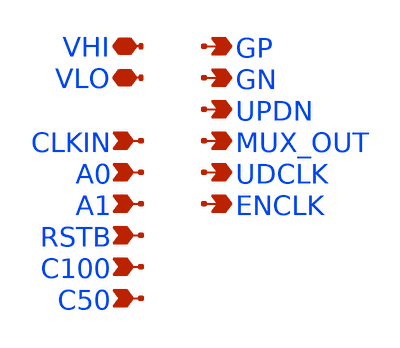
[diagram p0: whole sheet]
** sch_path: xschem/twcon_PEX.sch
**.subckt twcon_PEX VHI VLO UPDN CLKIN A0 A1 RSTB C100 C50 GP GN MUX_OUT UDCLK ENCLK
*.iopin VHI
*.iopin VLO
*.opin UPDN
*.ipin CLKIN
*.ipin A0
*.ipin A1
*.ipin RSTB
*.ipin C100
*.ipin C50
*.opin GP
*.opin GN
*.opin MUX_OUT
*.opin UDCLK
*.opin ENCLK
**** begin user architecture code

* NGSPICE file created from twcon.ext - technology: sky130A
.subckt twcon VHI VLO UPDN CLKIN A0 A1 GP GN RSTB C100 C50 MUX_OUT UDCLK ENCLK

* NGSPICE file created from twcon_flat.ext - technology: sky130A

X0 a_533_410# VLO VLO VLO sky130_fd_pr__nfet_01v8_lvt ad=0p pd=0u as=0p ps=0u w=420000u l=150000u
X1 VLO a_533_410# a_555_119# VLO sky130_fd_pr__nfet_01v8_lvt ad=0p pd=0u as=0p ps=0u w=420000u
+ l=150000u
X2 a_1346_464# a_1060_368# a_1262_464# w_n2918_628# sky130_fd_pr__pfet_01v8 ad=0p pd=0u as=0p ps=0u
+ w=420000u l=150000u
X3 VHI VLO VHI w_n2918_1664# sky130_fd_pr__pfet_01v8 ad=0p pd=0u as=0p ps=0u w=1e+06u l=1e+06u
X4 a_1377_125# a_1199_366# VLO VLO sky130_fd_pr__nfet_01v8_lvt ad=0p pd=0u as=0p ps=0u w=420000u
+ l=150000u
X5 a_n2680_1700# a_n1984_1467# VLO sky130_fd_pr__res_xhigh_po_1p41 l=500000u
X6 a_2189_82# a_1060_368# a_2178_424# w_n2918_628# sky130_fd_pr__pfet_01v8 ad=0p pd=0u as=0p ps=0u
+ w=840000u l=150000u
X7 VHI VLO a_219_464# w_n2918_628# sky130_fd_pr__pfet_01v8 ad=0p pd=0u as=0p ps=0u w=640000u
+ l=150000u
X8 a_n1326_740# a_n1984_915# VHI w_n2918_628# sky130_fd_pr__pfet_01v8 ad=0p pd=0u as=0p ps=0u
+ w=1.12e+06u l=150000u
X9 a_2363_740# a_880_1086# a_2189_1140# w_n2918_628# sky130_fd_pr__pfet_01v8 ad=0p pd=0u as=0p ps=0u
+ w=420000u l=150000u
X10 VHI a_3464_1110# a_3664_740# w_n2918_628# sky130_fd_pr__pfet_01v8 ad=0p pd=0u as=0p ps=0u
+ w=1.12e+06u l=150000u
X11 MUX_OUT a_n848_1110# VLO VLO sky130_fd_pr__nfet_01v8_lvt ad=0p pd=0u as=0p ps=0u w=740000u
+ l=150000u
X12 VHI A0 a_n1326_740# w_n2918_628# sky130_fd_pr__pfet_01v8 ad=0p pd=0u as=0p ps=0u w=1.12e+06u
+ l=150000u
X13 a_1262_464# a_1199_366# VHI w_n2918_628# sky130_fd_pr__pfet_01v8 ad=0p pd=0u as=0p ps=0u
+ w=420000u l=150000u
X14 a_3664_740# a_3464_1110# VHI w_n2918_628# sky130_fd_pr__pfet_01v8 ad=0p pd=0u as=0p ps=0u
+ w=1.12e+06u l=150000u
X15 VHI VLO VHI w_n2918_1664# sky130_fd_pr__pfet_01v8 ad=0p pd=0u as=0p ps=0u w=1e+06u l=1e+06u
X16 VLO VHI VLO VLO sky130_fd_pr__nfet_01v8_lvt ad=0p pd=0u as=0p ps=0u w=420000u l=1e+06u
X17 a_4149_409# a_n1069_979# a_4146_119# VLO sky130_fd_pr__nfet_01v8_lvt ad=0p pd=0u as=0p ps=0u
+ w=640000u l=150000u
X18 VLO UPDN a_4059_1110# VLO sky130_fd_pr__nfet_01v8_lvt ad=0p pd=0u as=0p ps=0u w=740000u
+ l=150000u
X19 a_2189_82# a_880_98# a_2094_125# VLO sky130_fd_pr__nfet_01v8_lvt ad=0p pd=0u as=0p ps=0u
+ w=550000u l=150000u
X20 a_n1750_2358# a_n1984_915# sky130_fd_pr__cap_mim_m3_2 l=1.6e+06u w=1.57e+07u
X21 GN a_4149_409# VLO VLO sky130_fd_pr__nfet_01v8_lvt ad=0p pd=0u as=0p ps=0u w=740000u l=150000u
X22 a_n1323_1406# a_n1984_1467# VLO VLO sky130_fd_pr__nfet_01v8_lvt ad=0p pd=0u as=0p ps=0u
+ w=740000u l=150000u
X23 a_219_740# a_533_883# a_389_1129# w_n2918_628# sky130_fd_pr__pfet_01v8 ad=0p pd=0u as=0p ps=0u
+ w=640000u l=150000u
X24 a_389_1129# VLO a_311_1129# VLO sky130_fd_pr__nfet_01v8_lvt ad=0p pd=0u as=0p ps=0u w=420000u
+ l=150000u
X25 a_1060_740# a_880_1086# VLO VLO sky130_fd_pr__nfet_01v8_lvt ad=0p pd=0u as=0p ps=0u w=740000u
+ l=150000u
X26 a_2189_1140# a_1060_740# a_2178_740# w_n2918_628# sky130_fd_pr__pfet_01v8 ad=0p pd=0u as=0p
+ ps=0u w=840000u l=150000u
X27 a_2408_839# a_2189_1140# a_2748_740# w_n2918_628# sky130_fd_pr__pfet_01v8 ad=0p pd=0u as=0p
+ ps=0u w=1e+06u l=150000u
X28 a_n1528_368# CLKIN VHI w_n2918_628# sky130_fd_pr__pfet_01v8 ad=0p pd=0u as=0p ps=0u w=1.12e+06u
+ l=150000u
X29 a_n832_135# a_n1313_n698# sky130_fd_pr__cap_mim_m3_1 l=1.6e+06u w=7.85e+06u
X30 a_4146_119# a_3664_740# VLO VLO sky130_fd_pr__nfet_01v8_lvt ad=0p pd=0u as=0p ps=0u w=640000u
+ l=150000u
X31 a_555_119# a_n1069_979# a_389_119# VLO sky130_fd_pr__nfet_01v8_lvt ad=0p pd=0u as=0p ps=0u
+ w=420000u l=150000u
X32 VHI a_n1125_796# a_n628_764# w_n2918_628# sky130_fd_pr__pfet_01v8 ad=0p pd=0u as=0p ps=0u
+ w=1e+06u l=150000u
X33 a_n709_1110# a_n1326_740# a_n848_1110# VLO sky130_fd_pr__nfet_01v8_lvt ad=0p pd=0u as=0p ps=0u
+ w=740000u l=150000u
X34 a_389_1129# VHI a_398_740# w_n2918_628# sky130_fd_pr__pfet_01v8 ad=0p pd=0u as=0p ps=0u
+ w=640000u l=150000u
X35 a_4059_1110# a_3664_740# GP VLO sky130_fd_pr__nfet_01v8_lvt ad=0p pd=0u as=0p ps=0u w=740000u
+ l=150000u
X36 VLO VHI a_1665_73# VLO sky130_fd_pr__nfet_01v8_lvt ad=0p pd=0u as=0p ps=0u w=550000u l=150000u
X37 a_2178_424# a_1199_366# VHI w_n2918_628# sky130_fd_pr__pfet_01v8 ad=0p pd=0u as=0p ps=0u
+ w=840000u l=150000u
X38 VHI UPDN GP w_n2918_628# sky130_fd_pr__pfet_01v8 ad=0p pd=0u as=0p ps=0u w=1.12e+06u l=150000u
X39 VHI a_n1069_979# a_n1125_796# w_n2918_628# sky130_fd_pr__pfet_01v8 ad=0p pd=0u as=0p ps=0u
+ w=840000u l=150000u
X40 VLO a_3464_1110# a_3664_740# VLO sky130_fd_pr__nfet_01v8_lvt ad=0p pd=0u as=0p ps=0u w=740000u
+ l=150000u
X41 VLO VHI VLO VLO sky130_fd_pr__nfet_01v8_lvt ad=0p pd=0u as=0p ps=0u w=420000u l=1e+06u
X42 a_4059_1110# UPDN VLO VLO sky130_fd_pr__nfet_01v8_lvt ad=0p pd=0u as=0p ps=0u w=740000u
+ l=150000u
X43 VHI VHI a_2408_839# w_n2918_628# sky130_fd_pr__pfet_01v8 ad=0p pd=0u as=0p ps=0u w=1e+06u
+ l=150000u
X44 VLO C100 a_n1750_3072# VLO sky130_fd_pr__nfet_01v8 ad=0p pd=0u as=0p ps=0u w=2e+06u l=150000u
X45 VLO a_2408_839# a_3464_1110# VLO sky130_fd_pr__nfet_01v8_lvt ad=0p pd=0u as=0p ps=0u w=640000u
+ l=150000u
X46 a_n832_135# a_n1313_n1412# sky130_fd_pr__cap_mim_m3_1 l=1.6e+06u w=1.57e+07u
X47 a_n1069_979# a_2408_410# VLO VLO sky130_fd_pr__nfet_01v8_lvt ad=0p pd=0u as=0p ps=0u w=740000u
+ l=150000u
X48 VHI A1 a_n1326_1700# w_n2918_1664# sky130_fd_pr__pfet_01v8 ad=0p pd=0u as=0p ps=0u w=1.12e+06u
+ l=150000u
X49 VHI a_4149_409# GN w_n2918_628# sky130_fd_pr__pfet_01v8 ad=0p pd=0u as=0p ps=0u w=1.12e+06u
+ l=150000u
X50 VLO ENCLK a_880_1086# VLO sky130_fd_pr__nfet_01v8_lvt ad=0p pd=0u as=0p ps=0u w=740000u
+ l=150000u
X51 a_389_1129# a_880_1086# a_1346_784# w_n2918_628# sky130_fd_pr__pfet_01v8 ad=0p pd=0u as=0p ps=0u
+ w=640000u l=150000u
X52 VLO a_2408_839# a_3253_1110# VLO sky130_fd_pr__nfet_01v8_lvt ad=0p pd=0u as=0p ps=0u w=740000u
+ l=150000u
X53 VHI a_2408_839# a_3464_1110# w_n2918_628# sky130_fd_pr__pfet_01v8 ad=0p pd=0u as=0p ps=0u
+ w=1e+06u l=150000u
X54 a_n880_2358# C50 VLO VLO sky130_fd_pr__nfet_01v8 ad=0p pd=0u as=0p ps=0u w=2e+06u l=150000u
X55 VLO CLKIN ENCLK VLO sky130_fd_pr__nfet_01v8_lvt ad=0p pd=0u as=0p ps=0u w=740000u l=150000u
X56 a_2748_740# a_1835_923# VHI w_n2918_628# sky130_fd_pr__pfet_01v8 ad=0p pd=0u as=0p ps=0u
+ w=1e+06u l=150000u
X57 a_n1326_1700# A1 a_n1323_1406# VLO sky130_fd_pr__nfet_01v8_lvt ad=0p pd=0u as=0p ps=0u w=740000u
+ l=150000u
X58 VLO VHI VLO VLO sky130_fd_pr__nfet_01v8_lvt ad=0p pd=0u as=0p ps=0u w=420000u l=1e+06u
X59 VLO UPDN a_4059_1110# VLO sky130_fd_pr__nfet_01v8_lvt ad=0p pd=0u as=0p ps=0u w=740000u
+ l=150000u
X60 VHI MUX_OUT a_1835_923# w_n2918_628# sky130_fd_pr__pfet_01v8 ad=0p pd=0u as=0p ps=0u w=640000u
+ l=150000u
X61 VHI a_2408_839# a_3253_1110# w_n2918_628# sky130_fd_pr__pfet_01v8 ad=0p pd=0u as=0p ps=0u
+ w=1.12e+06u l=150000u
X62 VHI VLO VHI w_n2918_1664# sky130_fd_pr__pfet_01v8 ad=0p pd=0u as=0p ps=0u w=1e+06u l=1e+06u
X63 a_2178_740# a_1199_900# VHI w_n2918_628# sky130_fd_pr__pfet_01v8 ad=0p pd=0u as=0p ps=0u
+ w=840000u l=150000u
X64 a_n2680_1700# A1 VLO VLO sky130_fd_pr__nfet_01v8_lvt ad=0p pd=0u as=0p ps=0u w=740000u l=150000u
X65 VLO VHI VLO VLO sky130_fd_pr__nfet_01v8_lvt ad=0p pd=0u as=0p ps=0u w=420000u l=1e+06u
X66 a_2644_74# VHI VLO VLO sky130_fd_pr__nfet_01v8_lvt ad=0p pd=0u as=0p ps=0u w=740000u l=150000u
X67 a_n1326_1700# a_n1984_1467# VHI w_n2918_1664# sky130_fd_pr__pfet_01v8 ad=0p pd=0u as=0p ps=0u
+ w=1.12e+06u l=150000u
X68 VLO VHI VLO VLO sky130_fd_pr__nfet_01v8_lvt ad=0p pd=0u as=0p ps=0u w=420000u l=1e+06u
X69 VHI a_3664_740# a_4149_409# w_n2918_628# sky130_fd_pr__pfet_01v8 ad=0p pd=0u as=0p ps=0u
+ w=840000u l=150000u
X70 VLO VHI VLO VLO sky130_fd_pr__nfet_01v8_lvt ad=0p pd=0u as=0p ps=0u w=420000u l=1e+06u
X71 a_n628_764# a_n1326_1700# a_n848_1110# w_n2918_628# sky130_fd_pr__pfet_01v8 ad=0p pd=0u as=0p
+ ps=0u w=1e+06u l=150000u
X72 a_3253_1110# a_2408_839# VHI w_n2918_628# sky130_fd_pr__pfet_01v8 ad=0p pd=0u as=0p ps=0u
+ w=1.12e+06u l=150000u
X73 UDCLK CLKIN a_n171_74# VLO sky130_fd_pr__nfet_01v8_lvt ad=0p pd=0u as=0p ps=0u w=740000u
+ l=150000u
X74 a_398_740# VLO VHI w_n2918_628# sky130_fd_pr__pfet_01v8 ad=0p pd=0u as=0p ps=0u w=640000u
+ l=150000u
X75 a_n1984_1467# a_n880_3072# sky130_fd_pr__cap_mim_m3_1 l=1.6e+06u w=7.85e+06u
X76 VLO VHI VLO VLO sky130_fd_pr__nfet_01v8_lvt ad=0p pd=0u as=0p ps=0u w=420000u l=1e+06u
X77 ENCLK CLKIN VHI w_n2918_628# sky130_fd_pr__pfet_01v8 ad=0p pd=0u as=0p ps=0u w=1.12e+06u
+ l=150000u
X78 a_2408_839# a_1835_923# a_2644_1110# VLO sky130_fd_pr__nfet_01v8_lvt ad=0p pd=0u as=0p ps=0u
+ w=740000u l=150000u
X79 VLO VHI VLO VLO sky130_fd_pr__nfet_01v8_lvt ad=0p pd=0u as=0p ps=0u w=420000u l=1e+06u
X80 ENCLK CLKIN VLO VLO sky130_fd_pr__nfet_01v8_lvt ad=0p pd=0u as=0p ps=0u w=740000u l=150000u
X81 a_4059_1110# UPDN VLO VLO sky130_fd_pr__nfet_01v8_lvt ad=0p pd=0u as=0p ps=0u w=740000u
+ l=150000u
X82 a_n1313_n698# a_n832_135# sky130_fd_pr__cap_mim_m3_2 l=1.6e+06u w=7.85e+06u
X83 VHI VLO a_219_740# w_n2918_628# sky130_fd_pr__pfet_01v8 ad=0p pd=0u as=0p ps=0u w=640000u
+ l=150000u
X84 a_3664_740# a_3464_1110# VLO VLO sky130_fd_pr__nfet_01v8_lvt ad=0p pd=0u as=0p ps=0u w=740000u
+ l=150000u
X85 VHI CLKIN ENCLK w_n2918_628# sky130_fd_pr__pfet_01v8 ad=0p pd=0u as=0p ps=0u w=1.12e+06u
+ l=150000u
X86 GP a_3664_740# a_4059_1110# VLO sky130_fd_pr__nfet_01v8_lvt ad=0p pd=0u as=0p ps=0u w=740000u
+ l=150000u
X87 VLO VHI VLO VLO sky130_fd_pr__nfet_01v8_lvt ad=0p pd=0u as=0p ps=0u w=420000u l=1e+06u
X88 VHI a_3464_94# UPDN w_n2918_628# sky130_fd_pr__pfet_01v8 ad=0p pd=0u as=0p ps=0u w=1.12e+06u
+ l=150000u
X89 a_n848_1110# a_n1326_740# a_n929_764# w_n2918_628# sky130_fd_pr__pfet_01v8 ad=0p pd=0u as=0p
+ ps=0u w=1e+06u l=150000u
X90 VLO a_2408_410# a_n1069_979# VLO sky130_fd_pr__nfet_01v8_lvt ad=0p pd=0u as=0p ps=0u w=740000u
+ l=150000u
X91 a_1060_368# a_880_98# VLO VLO sky130_fd_pr__nfet_01v8_lvt ad=0p pd=0u as=0p ps=0u w=740000u
+ l=150000u
X92 VHI VLO VHI w_n2918_1664# sky130_fd_pr__pfet_01v8 ad=0p pd=0u as=0p ps=0u w=1e+06u l=1e+06u
X93 a_2189_1140# a_880_1086# a_2094_1097# VLO sky130_fd_pr__nfet_01v8_lvt ad=0p pd=0u as=0p ps=0u
+ w=550000u l=150000u
X94 a_2644_1110# a_2189_1140# a_2408_839# VLO sky130_fd_pr__nfet_01v8_lvt ad=0p pd=0u as=0p ps=0u
+ w=740000u l=150000u
X95 VHI RSTB a_1835_257# w_n2918_628# sky130_fd_pr__pfet_01v8 ad=0p pd=0u as=0p ps=0u w=640000u
+ l=150000u
X96 a_n1313_n1412# a_n832_135# sky130_fd_pr__cap_mim_m3_2 l=1.6e+06u w=1.57e+07u
X97 UPDN a_3464_94# VHI w_n2918_628# sky130_fd_pr__pfet_01v8 ad=0p pd=0u as=0p ps=0u w=1.12e+06u
+ l=150000u
X98 a_3253_1110# a_2408_839# VLO VLO sky130_fd_pr__nfet_01v8_lvt ad=0p pd=0u as=0p ps=0u w=740000u
+ l=150000u
X99 VHI VLO VHI w_n2918_1664# sky130_fd_pr__pfet_01v8 ad=0p pd=0u as=0p ps=0u w=1e+06u l=1e+06u
X100 VLO a_533_883# a_555_1129# VLO sky130_fd_pr__nfet_01v8_lvt ad=0p pd=0u as=0p ps=0u w=420000u
+ l=150000u
X101 a_2439_82# a_1060_368# a_2189_82# VLO sky130_fd_pr__nfet_01v8_lvt ad=0p pd=0u as=0p ps=0u
+ w=420000u l=150000u
X102 a_1377_1123# a_1199_900# VLO VLO sky130_fd_pr__nfet_01v8_lvt ad=0p pd=0u as=0p ps=0u w=420000u
+ l=150000u
X103 a_1346_784# a_1060_740# a_1262_784# w_n2918_628# sky130_fd_pr__pfet_01v8 ad=0p pd=0u as=0p
+ ps=0u w=420000u l=150000u
X104 a_n1313_n1412# C100 VLO VLO sky130_fd_pr__nfet_01v8 ad=0p pd=0u as=0p ps=0u w=2e+06u l=150000u
X105 VHI a_2408_410# a_2363_508# w_n2918_628# sky130_fd_pr__pfet_01v8 ad=0p pd=0u as=0p ps=0u
+ w=420000u l=150000u
X106 VLO UDCLK a_880_98# VLO sky130_fd_pr__nfet_01v8_lvt ad=0p pd=0u as=0p ps=0u w=740000u l=150000u
X107 a_n880_3072# C100 VLO VLO sky130_fd_pr__nfet_01v8 ad=0p pd=0u as=0p ps=0u w=2e+06u l=150000u
X108 a_n880_3072# a_n1984_1467# sky130_fd_pr__cap_mim_m3_2 l=1.6e+06u w=7.85e+06u
X109 a_2408_410# a_2189_82# a_2748_392# w_n2918_628# sky130_fd_pr__pfet_01v8 ad=0p pd=0u as=0p ps=0u
+ w=1e+06u l=150000u
X110 a_311_1129# VLO VLO VLO sky130_fd_pr__nfet_01v8_lvt ad=0p pd=0u as=0p ps=0u w=420000u l=150000u
X111 MUX_OUT a_n848_1110# VHI w_n2918_628# sky130_fd_pr__pfet_01v8 ad=0p pd=0u as=0p ps=0u
+ w=1.12e+06u l=150000u
X112 a_1262_784# a_1199_900# VHI w_n2918_628# sky130_fd_pr__pfet_01v8 ad=0p pd=0u as=0p ps=0u
+ w=420000u l=150000u
X113 a_533_410# VLO VHI w_n2918_628# sky130_fd_pr__pfet_01v8 ad=0p pd=0u as=0p ps=0u w=640000u
+ l=150000u
X114 a_n1984_1467# a_n880_2358# sky130_fd_pr__cap_mim_m3_1 l=1.6e+06u w=1.57e+07u
X115 a_1199_366# a_1346_464# a_1665_73# VLO sky130_fd_pr__nfet_01v8_lvt ad=0p pd=0u as=0p ps=0u
+ w=550000u l=150000u
X116 a_555_1129# VHI a_389_1129# VLO sky130_fd_pr__nfet_01v8_lvt ad=0p pd=0u as=0p ps=0u w=420000u
+ l=150000u
X117 VHI VHI a_2408_410# w_n2918_628# sky130_fd_pr__pfet_01v8 ad=0p pd=0u as=0p ps=0u w=1e+06u
+ l=150000u
X118 VHI a_1835_257# a_1784_424# w_n2918_628# sky130_fd_pr__pfet_01v8 ad=0p pd=0u as=0p ps=0u
+ w=840000u l=150000u
X119 a_n1528_368# CLKIN VLO VLO sky130_fd_pr__nfet_01v8_lvt ad=0p pd=0u as=0p ps=0u w=740000u
+ l=150000u
X120 a_n2680_740# A0 VHI w_n2918_628# sky130_fd_pr__pfet_01v8 ad=0p pd=0u as=0p ps=0u w=1.12e+06u
+ l=150000u
X121 a_n929_764# a_n1069_979# VHI w_n2918_628# sky130_fd_pr__pfet_01v8 ad=0p pd=0u as=0p ps=0u
+ w=1e+06u l=150000u
X122 a_2644_1110# VHI VLO VLO sky130_fd_pr__nfet_01v8_lvt ad=0p pd=0u as=0p ps=0u w=740000u
+ l=150000u
X123 a_2644_74# a_2189_82# a_2408_410# VLO sky130_fd_pr__nfet_01v8_lvt ad=0p pd=0u as=0p ps=0u
+ w=740000u l=150000u
X124 a_n2680_740# a_n1984_915# VLO sky130_fd_pr__res_xhigh_po_1p41 l=500000u
X125 a_1346_784# a_880_1086# a_1377_1123# VLO sky130_fd_pr__nfet_01v8_lvt ad=0p pd=0u as=0p ps=0u
+ w=420000u l=150000u
X126 a_2439_1166# a_1060_740# a_2189_1140# VLO sky130_fd_pr__nfet_01v8_lvt ad=0p pd=0u as=0p ps=0u
+ w=420000u l=150000u
X127 GN a_4149_409# VHI w_n2918_628# sky130_fd_pr__pfet_01v8 ad=0p pd=0u as=0p ps=0u w=1.12e+06u
+ l=150000u
X128 VHI ENCLK a_880_1086# w_n2918_628# sky130_fd_pr__pfet_01v8 ad=0p pd=0u as=0p ps=0u w=1.12e+06u
+ l=150000u
X129 VHI a_2408_410# a_n1069_979# w_n2918_628# sky130_fd_pr__pfet_01v8 ad=0p pd=0u as=0p ps=0u
+ w=1.12e+06u l=150000u
X130 a_2363_508# a_880_98# a_2189_82# w_n2918_628# sky130_fd_pr__pfet_01v8 ad=0p pd=0u as=0p ps=0u
+ w=420000u l=150000u
X131 a_n1313_n698# C50 VLO VLO sky130_fd_pr__nfet_01v8 ad=0p pd=0u as=0p ps=0u w=2e+06u l=150000u
X132 a_4059_1110# a_3664_740# GP VLO sky130_fd_pr__nfet_01v8_lvt ad=0p pd=0u as=0p ps=0u w=740000u
+ l=150000u
X133 a_n1984_915# a_n1750_3072# sky130_fd_pr__cap_mim_m3_1 l=1.6e+06u w=7.85e+06u
X134 UPDN a_3464_94# VLO VLO sky130_fd_pr__nfet_01v8_lvt ad=0p pd=0u as=0p ps=0u w=740000u l=150000u
X135 a_2748_392# a_1835_257# VHI w_n2918_628# sky130_fd_pr__pfet_01v8 ad=0p pd=0u as=0p ps=0u
+ w=1e+06u l=150000u
X136 a_2094_125# a_1199_366# VLO VLO sky130_fd_pr__nfet_01v8_lvt ad=0p pd=0u as=0p ps=0u w=550000u
+ l=150000u
X137 VHI VLO VHI w_n2918_1664# sky130_fd_pr__pfet_01v8 ad=0p pd=0u as=0p ps=0u w=1e+06u l=1e+06u
X138 a_n1069_979# a_2408_410# VHI w_n2918_628# sky130_fd_pr__pfet_01v8 ad=0p pd=0u as=0p ps=0u
+ w=1.12e+06u l=150000u
X139 a_1060_740# a_880_1086# VHI w_n2918_628# sky130_fd_pr__pfet_01v8 ad=0p pd=0u as=0p ps=0u
+ w=1.12e+06u l=150000u
X140 a_1784_424# a_1346_464# a_1199_366# w_n2918_628# sky130_fd_pr__pfet_01v8 ad=0p pd=0u as=0p
+ ps=0u w=840000u l=150000u
X141 a_389_1129# a_1060_740# a_1346_784# VLO sky130_fd_pr__nfet_01v8_lvt ad=0p pd=0u as=0p ps=0u
+ w=420000u l=150000u
X142 VLO RSTB a_1835_257# VLO sky130_fd_pr__nfet_01v8_lvt ad=0p pd=0u as=0p ps=0u w=420000u
+ l=150000u
X143 UDCLK a_n832_135# VHI w_n2918_628# sky130_fd_pr__pfet_01v8 ad=0p pd=0u as=0p ps=0u w=1.12e+06u
+ l=150000u
X144 a_1199_366# VHI VHI w_n2918_628# sky130_fd_pr__pfet_01v8 ad=0p pd=0u as=0p ps=0u w=840000u
+ l=150000u
X145 VLO MUX_OUT a_1835_923# VLO sky130_fd_pr__nfet_01v8_lvt ad=0p pd=0u as=0p ps=0u w=420000u
+ l=150000u
X146 VLO VHI a_1665_1097# VLO sky130_fd_pr__nfet_01v8_lvt ad=0p pd=0u as=0p ps=0u w=550000u
+ l=150000u
X147 VHI a_1835_923# a_1784_740# w_n2918_628# sky130_fd_pr__pfet_01v8 ad=0p pd=0u as=0p ps=0u
+ w=840000u l=150000u
X148 a_389_119# VLO a_311_119# VLO sky130_fd_pr__nfet_01v8_lvt ad=0p pd=0u as=0p ps=0u w=420000u
+ l=150000u
X149 a_n2680_1700# A1 VHI w_n2918_1664# sky130_fd_pr__pfet_01v8 ad=0p pd=0u as=0p ps=0u w=1.12e+06u
+ l=150000u
X150 VLO VHI VLO VLO sky130_fd_pr__nfet_01v8_lvt ad=0p pd=0u as=0p ps=0u w=420000u l=1e+06u
X151 a_1199_900# a_1346_784# a_1665_1097# VLO sky130_fd_pr__nfet_01v8_lvt ad=0p pd=0u as=0p ps=0u
+ w=550000u l=150000u
X152 GN a_4149_409# VLO VLO sky130_fd_pr__nfet_01v8_lvt ad=0p pd=0u as=0p ps=0u w=740000u l=150000u
X153 VHI CLKIN UDCLK w_n2918_628# sky130_fd_pr__pfet_01v8 ad=0p pd=0u as=0p ps=0u w=1.12e+06u
+ l=150000u
X154 a_n1323_1110# a_n1984_915# VLO VLO sky130_fd_pr__nfet_01v8_lvt ad=0p pd=0u as=0p ps=0u
+ w=740000u l=150000u
X155 VLO a_2408_839# a_2439_1166# VLO sky130_fd_pr__nfet_01v8_lvt ad=0p pd=0u as=0p ps=0u w=420000u
+ l=150000u
X156 a_4149_409# a_n1069_979# VHI w_n2918_628# sky130_fd_pr__pfet_01v8 ad=0p pd=0u as=0p ps=0u
+ w=840000u l=150000u
X157 VHI VLO VHI w_n2918_1664# sky130_fd_pr__pfet_01v8 ad=0p pd=0u as=0p ps=0u w=1e+06u l=1e+06u
X158 VHI VLO VHI w_n2918_1664# sky130_fd_pr__pfet_01v8 ad=0p pd=0u as=0p ps=0u w=1e+06u l=1e+06u
X159 GP UPDN VHI w_n2918_628# sky130_fd_pr__pfet_01v8 ad=0p pd=0u as=0p ps=0u w=1.12e+06u l=150000u
X160 VHI VLO VHI w_n2918_1664# sky130_fd_pr__pfet_01v8 ad=0p pd=0u as=0p ps=0u w=1e+06u l=1e+06u
X161 a_533_883# VLO VLO VLO sky130_fd_pr__nfet_01v8_lvt ad=0p pd=0u as=0p ps=0u w=420000u l=150000u
X162 a_1784_740# a_1346_784# a_1199_900# w_n2918_628# sky130_fd_pr__pfet_01v8 ad=0p pd=0u as=0p
+ ps=0u w=840000u l=150000u
X163 a_n880_2358# a_n1984_1467# sky130_fd_pr__cap_mim_m3_2 l=1.6e+06u w=1.57e+07u
X164 VHI VLO VHI w_n2918_1664# sky130_fd_pr__pfet_01v8 ad=0p pd=0u as=0p ps=0u w=1e+06u l=1e+06u
X165 VLO VHI VLO VLO sky130_fd_pr__nfet_01v8_lvt ad=0p pd=0u as=0p ps=0u w=420000u l=1e+06u
X166 a_1199_900# VHI VHI w_n2918_628# sky130_fd_pr__pfet_01v8 ad=0p pd=0u as=0p ps=0u w=840000u
+ l=150000u
X167 a_n171_74# a_n832_135# VLO VLO sky130_fd_pr__nfet_01v8_lvt ad=0p pd=0u as=0p ps=0u w=740000u
+ l=150000u
X168 a_1665_1097# a_1835_923# a_1199_900# VLO sky130_fd_pr__nfet_01v8_lvt ad=0p pd=0u as=0p ps=0u
+ w=550000u l=150000u
X169 a_2094_1097# a_1199_900# VLO VLO sky130_fd_pr__nfet_01v8_lvt ad=0p pd=0u as=0p ps=0u w=550000u
+ l=150000u
X170 VLO VHI VLO VLO sky130_fd_pr__nfet_01v8_lvt ad=0p pd=0u as=0p ps=0u w=420000u l=1e+06u
X171 VLO a_3664_740# a_4146_119# VLO sky130_fd_pr__nfet_01v8_lvt ad=0p pd=0u as=0p ps=0u w=640000u
+ l=150000u
X172 VHI VLO VHI w_n2918_1664# sky130_fd_pr__pfet_01v8 ad=0p pd=0u as=0p ps=0u w=1e+06u l=1e+06u
X173 a_311_119# VLO VLO VLO sky130_fd_pr__nfet_01v8_lvt ad=0p pd=0u as=0p ps=0u w=420000u l=150000u
X174 VLO a_3464_94# UPDN VLO sky130_fd_pr__nfet_01v8_lvt ad=0p pd=0u as=0p ps=0u w=740000u l=150000u
X175 a_219_464# a_533_410# a_389_119# w_n2918_628# sky130_fd_pr__pfet_01v8 ad=0p pd=0u as=0p ps=0u
+ w=640000u l=150000u
X176 VHI a_3664_740# GP w_n2918_628# sky130_fd_pr__pfet_01v8 ad=0p pd=0u as=0p ps=0u w=1.12e+06u
+ l=150000u
X177 VHI VLO VHI w_n2918_1664# sky130_fd_pr__pfet_01v8 ad=0p pd=0u as=0p ps=0u w=1e+06u l=1e+06u
X178 VLO VHI VLO VLO sky130_fd_pr__nfet_01v8_lvt ad=0p pd=0u as=0p ps=0u w=420000u l=1e+06u
X179 a_1665_73# a_1835_257# a_1199_366# VLO sky130_fd_pr__nfet_01v8_lvt ad=0p pd=0u as=0p ps=0u
+ w=550000u l=150000u
X180 a_n1750_3072# a_n1984_915# sky130_fd_pr__cap_mim_m3_2 l=1.6e+06u w=7.85e+06u
X181 VLO a_4149_409# GN VLO sky130_fd_pr__nfet_01v8_lvt ad=0p pd=0u as=0p ps=0u w=740000u l=150000u
X182 VLO VHI VLO VLO sky130_fd_pr__nfet_01v8_lvt ad=0p pd=0u as=0p ps=0u w=420000u l=1e+06u
X183 a_n1326_740# A0 a_n1323_1110# VLO sky130_fd_pr__nfet_01v8_lvt ad=0p pd=0u as=0p ps=0u w=740000u
+ l=150000u
X184 a_1346_464# a_880_98# a_1377_125# VLO sky130_fd_pr__nfet_01v8_lvt ad=0p pd=0u as=0p ps=0u
+ w=420000u l=150000u
X185 a_389_119# a_n1069_979# a_398_464# w_n2918_628# sky130_fd_pr__pfet_01v8 ad=0p pd=0u as=0p ps=0u
+ w=640000u l=150000u
X186 a_n2680_740# A0 VLO VLO sky130_fd_pr__nfet_01v8_lvt ad=0p pd=0u as=0p ps=0u w=740000u l=150000u
X187 VLO a_n1069_979# a_n1125_796# VLO sky130_fd_pr__nfet_01v8_lvt ad=0p pd=0u as=0p ps=0u w=550000u
+ l=150000u
X188 a_n926_1110# a_n1069_979# VLO VLO sky130_fd_pr__nfet_01v8_lvt ad=0p pd=0u as=0p ps=0u w=740000u
+ l=150000u
X189 VLO VHI VLO VLO sky130_fd_pr__nfet_01v8_lvt ad=0p pd=0u as=0p ps=0u w=420000u l=1e+06u
X190 VLO a_n1125_796# a_n709_1110# VLO sky130_fd_pr__nfet_01v8_lvt ad=0p pd=0u as=0p ps=0u w=740000u
+ l=150000u
X191 GP a_3664_740# VHI w_n2918_628# sky130_fd_pr__pfet_01v8 ad=0p pd=0u as=0p ps=0u w=1.12e+06u
+ l=150000u
X192 VHI VLO VHI w_n2918_1664# sky130_fd_pr__pfet_01v8 ad=0p pd=0u as=0p ps=0u w=1e+06u l=1e+06u
X193 a_533_883# VLO VHI w_n2918_628# sky130_fd_pr__pfet_01v8 ad=0p pd=0u as=0p ps=0u w=640000u
+ l=150000u
X194 VHI a_4149_409# GN w_n2918_628# sky130_fd_pr__pfet_01v8 ad=0p pd=0u as=0p ps=0u w=1.12e+06u
+ l=150000u
X195 a_2408_410# a_1835_257# a_2644_74# VLO sky130_fd_pr__nfet_01v8_lvt ad=0p pd=0u as=0p ps=0u
+ w=740000u l=150000u
X196 VHI a_2408_410# a_3464_94# w_n2918_628# sky130_fd_pr__pfet_01v8 ad=0p pd=0u as=0p ps=0u
+ w=1e+06u l=150000u
X197 VHI a_2408_839# a_2363_740# w_n2918_628# sky130_fd_pr__pfet_01v8 ad=0p pd=0u as=0p ps=0u
+ w=420000u l=150000u
X198 VHI a_n1069_979# a_4149_409# w_n2918_628# sky130_fd_pr__pfet_01v8 ad=0p pd=0u as=0p ps=0u
+ w=840000u l=150000u
X199 VLO a_4149_409# GN VLO sky130_fd_pr__nfet_01v8_lvt ad=0p pd=0u as=0p ps=0u w=740000u l=150000u
X200 a_4146_119# a_n1069_979# a_4149_409# VLO sky130_fd_pr__nfet_01v8_lvt ad=0p pd=0u as=0p ps=0u
+ w=640000u l=150000u
X201 VLO a_2408_410# a_3464_94# VLO sky130_fd_pr__nfet_01v8_lvt ad=0p pd=0u as=0p ps=0u w=640000u
+ l=150000u
X202 a_389_119# a_880_98# a_1346_464# w_n2918_628# sky130_fd_pr__pfet_01v8 ad=0p pd=0u as=0p ps=0u
+ w=640000u l=150000u
X203 a_n1984_915# a_n1750_2358# sky130_fd_pr__cap_mim_m3_1 l=1.6e+06u w=1.57e+07u
X204 GN a_4149_409# VHI w_n2918_628# sky130_fd_pr__pfet_01v8 ad=0p pd=0u as=0p ps=0u w=1.12e+06u
+ l=150000u
X205 GP a_3664_740# a_4059_1110# VLO sky130_fd_pr__nfet_01v8_lvt ad=0p pd=0u as=0p ps=0u w=740000u
+ l=150000u
X206 a_389_119# a_1060_368# a_1346_464# VLO sky130_fd_pr__nfet_01v8_lvt ad=0p pd=0u as=0p ps=0u
+ w=420000u l=150000u
X207 VLO a_2408_410# a_2439_82# VLO sky130_fd_pr__nfet_01v8_lvt ad=0p pd=0u as=0p ps=0u w=420000u
+ l=150000u
X208 a_4149_409# a_3664_740# VHI w_n2918_628# sky130_fd_pr__pfet_01v8 ad=0p pd=0u as=0p ps=0u
+ w=840000u l=150000u
X209 VHI UDCLK a_880_98# w_n2918_628# sky130_fd_pr__pfet_01v8 ad=0p pd=0u as=0p ps=0u w=1.12e+06u
+ l=150000u
X210 VLO C50 a_n1750_2358# VLO sky130_fd_pr__nfet_01v8 ad=0p pd=0u as=0p ps=0u w=2e+06u l=150000u
X211 VHI VLO VHI w_n2918_1664# sky130_fd_pr__pfet_01v8 ad=0p pd=0u as=0p ps=0u w=1e+06u l=1e+06u
X212 VHI VLO VHI w_n2918_1664# sky130_fd_pr__pfet_01v8 ad=0p pd=0u as=0p ps=0u w=1e+06u l=1e+06u
X213 a_1060_368# a_880_98# VHI w_n2918_628# sky130_fd_pr__pfet_01v8 ad=0p pd=0u as=0p ps=0u
+ w=1.12e+06u l=150000u
X214 a_398_464# VLO VHI w_n2918_628# sky130_fd_pr__pfet_01v8 ad=0p pd=0u as=0p ps=0u w=640000u
+ l=150000u
X215 a_n1528_368# a_n832_135# VLO sky130_fd_pr__res_xhigh_po_1p41 l=500000u
X216 a_n848_1110# a_n1326_1700# a_n926_1110# VLO sky130_fd_pr__nfet_01v8_lvt ad=0p pd=0u as=0p ps=0u
+ w=740000u l=150000u
C0 a_n1313_n698# a_n832_135# 3.17fF
C1 a_n1069_979# VHI 2.11fF
C2 a_n1750_2358# a_n1984_915# 5.40fF
C3 a_n880_2358# a_n1984_1467# 5.51fF
C4 w_n2918_628# VHI 3.11fF
C5 VHI w_n2918_1664# 2.38fF
C6 a_n1984_915# a_n1750_3072# 2.84fF
C7 a_n880_3072# a_n1984_1467# 2.93fF
C8 a_n1313_n1412# a_n832_135# 5.41fF
C9 a_n1313_n1412# VLO 4.20fF $ **FLOATING
C10 a_n1313_n698# VLO 2.72fF $ **FLOATING
C11 a_n832_135# VLO 3.12fF $ **FLOATING
C12 a_n1984_915# VLO 2.51fF $ **FLOATING
C13 VHI VLO 18.50fF $ **FLOATING
C14 a_n1984_1467# VLO 2.36fF $ **FLOATING
C15 a_n880_2358# VLO 2.70fF $ **FLOATING
C16 a_n880_3072# VLO 2.64fF $ **FLOATING
C17 a_n1750_2358# VLO 2.66fF $ **FLOATING
C18 C50 VLO 2.81fF $ **FLOATING
C19 a_n1750_3072# VLO 2.53fF $ **FLOATING
C20 C100 VLO 3.36fF $ **FLOATING
C21 w_n2918_628# VLO 17.26fF $ **FLOATING
C22 w_n2918_1664# VLO 10.39fF $ **FLOATING



.ends


XDUT VHI VLO UPDN CLKIN A0 A1 GP GN RSTB C100 C50 MUX_OUT UDCLK ENCLK twcon


**** end user architecture code
**.ends
.end
